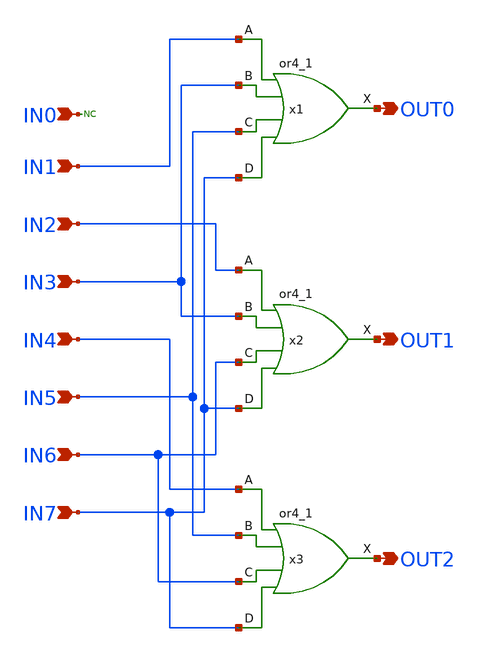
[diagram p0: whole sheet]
** sch_path: PriorityEncoder/8to3_Priority_Encoder_NOEI_v0p1p1.sch
.lib $::SKYWATER_MODELS/sky130.lib.spice tt
.include $::SKYWATER_STDCELLS/sky130_fd_sc_hd.spice

**.subckt 8to3_Priority_Encoder_NOEI_v0p1p1 IN0 IN1 IN2 IN3 IN4 IN5 IN6 IN7 OUT0 OUT1 OUT2
*.ipin IN0
*.ipin IN1
*.ipin IN2
*.ipin IN3
*.ipin IN4
*.ipin IN5
*.ipin IN6
*.ipin IN7
*.opin OUT0
*.opin OUT1
*.opin OUT2
.lib $::SKYWATER_MODELS/sky130.lib.spice tt
.include $::SKYWATER_STDCELLS/sky130_fd_sc_hd.spice

x1 IN1 IN3 IN5 IN7 GND GND VDD VDD OUT0 sky130_fd_sc_hd__or4_1
x2 IN2 IN3 IN6 IN7 GND GND VDD VDD OUT1 sky130_fd_sc_hd__or4_1
x3 IN4 IN5 IN6 IN7 GND GND VDD VDD OUT2 sky130_fd_sc_hd__or4_1
**.ends
.end
